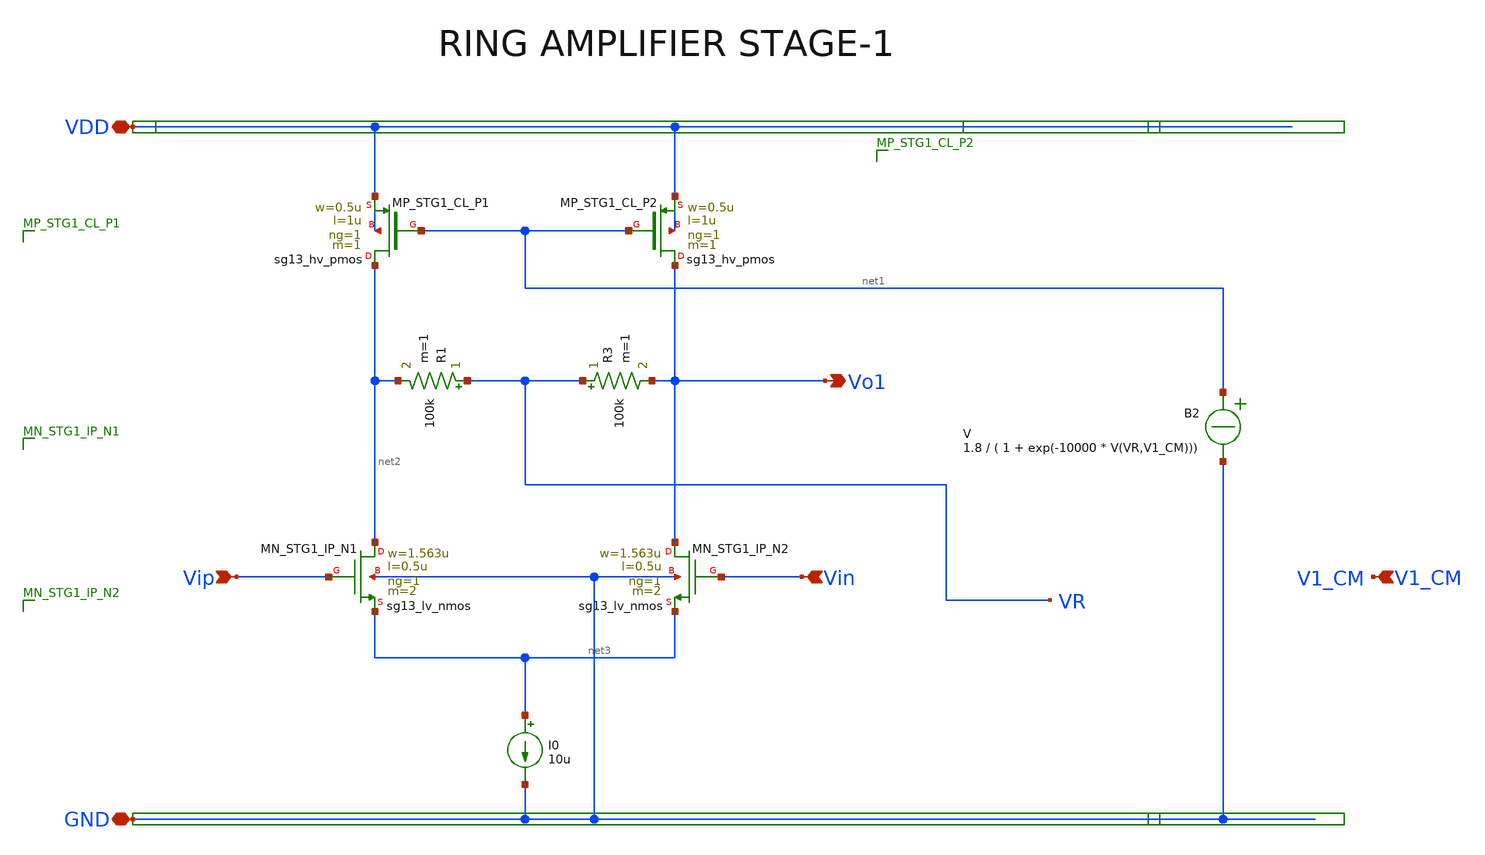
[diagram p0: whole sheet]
** sch_path: Design Files/RAMP/Fully-Diff-RAMP/STG1_2.sch
**.subckt STG1_2 VDD GND Vo1 Vip Vin V1_CM
*.iopin VDD
*.iopin GND
*.opin Vo1
*.ipin Vip
*.ipin Vin
*.ipin V1_CM
R1 VR net2 100k m=1
R3 VR Vo1 100k m=1
XMN_STG1_IP_N1 net2 Vip net3 GND sg13_lv_nmos w=1.563u l=0.5u ng=1 m=2 mm_ok=1
XMN_STG1_IP_N2 Vo1 Vin net3 GND sg13_lv_nmos w=1.563u l=0.5u ng=1 m=2 mm_ok=1
I0 net3 GND 10u
XMP_STG1_CL_P1 net2 net1 VDD VDD sg13_hv_pmos w=0.5u l=1u ng=1 m=1 mm_ok=1
XMP_STG1_CL_P2 Vo1 net1 VDD VDD sg13_hv_pmos w=0.5u l=1u ng=1 m=1 mm_ok=1
B2 net1 GND V = 1.8 / ( 1 + exp(-10000 * V(VR,V1_CM)))
**.ends
.end
